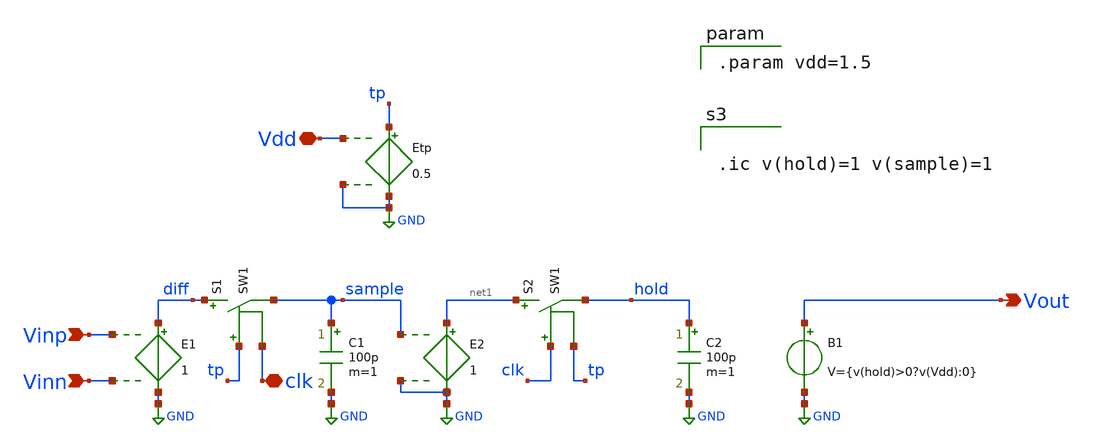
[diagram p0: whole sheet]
** sch_path: DSM_2ndOrder/1_Schematics/Ideal_Schematic/xschem/ideal_comparator.sch
**.subckt ideal_comparator Vinp Vinn Vout Vdd clk
*.ipin Vinp
*.ipin Vinn
*.opin Vout
*.iopin Vdd
*.iopin clk
E1 diff GND Vinp Vinn 1
S1 diff sample tp clk SW1
E2 net1 GND sample GND 1
C1 sample GND 100p m=1
S2 net1 hold clk tp SW1
C2 hold GND 100p m=1
B1 Vout GND V={v(hold)>0?v(Vdd):0}
Etp tp GND Vdd GND 0.5
**** begin user architecture code


.ic v(hold)=1 v(sample)=1



.param vdd=1.5

**** end user architecture code
**.ends
.GLOBAL GND
**** begin user architecture code
.MODEL SW1 SW( VT=0.1 VH=0.0 RON=0.01 ROFF=10G )
**** end user architecture code
.end
